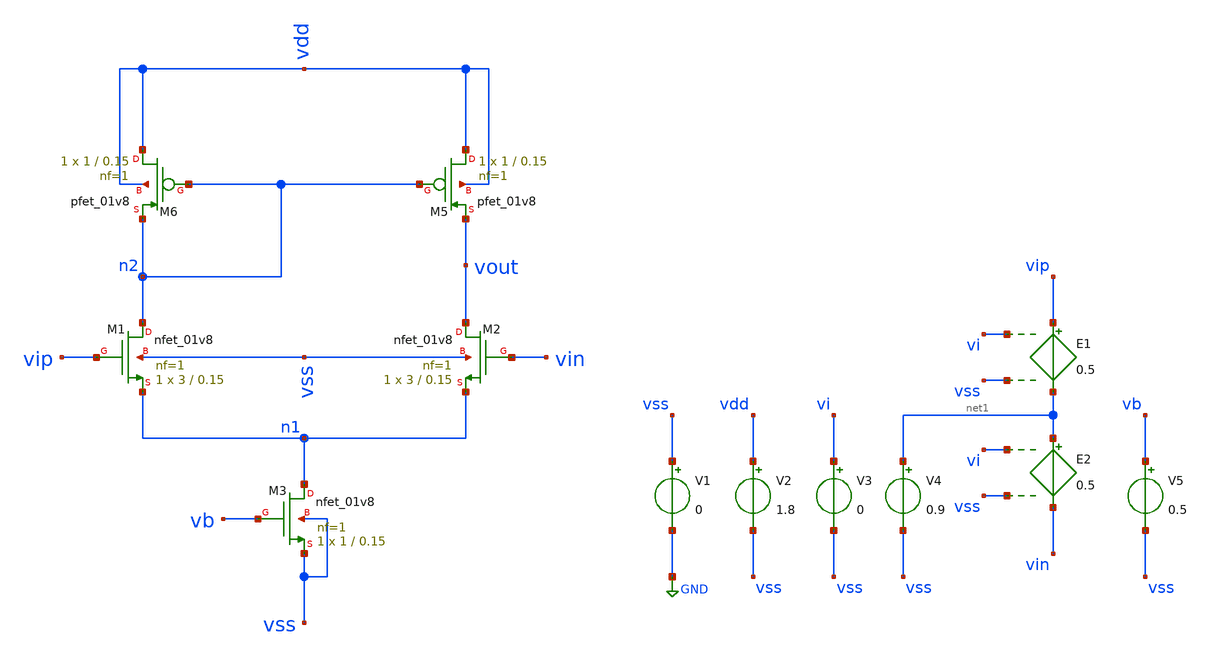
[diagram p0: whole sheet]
** sch_path: pre_layout_sim/ota_local_test.sch
**.subckt ota_local_test
XM1 n2 vip n1 vss sky130_fd_pr__nfet_01v8 L=0.15 W=3 nf=1 ad='int((1 + 1)/2) * 3 / 1 * 0.29' as='int((1 + 2)/2) * 3 / 1 * 0.29'
+ pd='2*int((1 + 1)/2) * (3 / 1 + 0.29)' ps='2*int((1 + 2)/2) * (3 / 1 + 0.29)' nrd='0.29 / 3 ' nrs='0.29 / 3 '
+ sa=0 sb=0 sd=0 mult=1 m=1
XM2 vout vin n1 vss sky130_fd_pr__nfet_01v8 L=0.15 W=3 nf=1 ad='int((1 + 1)/2) * 3 / 1 * 0.29' as='int((1 + 2)/2) * 3 / 1 * 0.29'
+ pd='2*int((1 + 1)/2) * (3 / 1 + 0.29)' ps='2*int((1 + 2)/2) * (3 / 1 + 0.29)' nrd='0.29 / 3 ' nrs='0.29 / 3 '
+ sa=0 sb=0 sd=0 mult=1 m=1
XM3 n1 vb vss vss sky130_fd_pr__nfet_01v8 L=0.15 W=1 nf=1 ad='int((1 + 1)/2) * 1 / 1 * 0.29' as='int((1 + 2)/2) * 1 / 1 * 0.29'
+ pd='2*int((1 + 1)/2) * (1 / 1 + 0.29)' ps='2*int((1 + 2)/2) * (1 / 1 + 0.29)' nrd='0.29 / 1 ' nrs='0.29 / 1 '
+ sa=0 sb=0 sd=0 mult=1 m=1
XM5 vdd n2 vout vdd sky130_fd_pr__pfet_01v8 L=0.15 W=1 nf=1 ad='int((1 + 1)/2) * 1 / 1 * 0.29' as='int((1 + 2)/2) * 1 / 1 * 0.29'
+ pd='2*int((1 + 1)/2) * (1 / 1 + 0.29)' ps='2*int((1 + 2)/2) * (1 / 1 + 0.29)' nrd='0.29 / 1 ' nrs='0.29 / 1 '
+ sa=0 sb=0 sd=0 mult=1 m=1
XM6 vdd n2 n2 vdd sky130_fd_pr__pfet_01v8 L=0.15 W=1 nf=1 ad='int((1 + 1)/2) * 1 / 1 * 0.29' as='int((1 + 2)/2) * 1 / 1 * 0.29'
+ pd='2*int((1 + 1)/2) * (1 / 1 + 0.29)' ps='2*int((1 + 2)/2) * (1 / 1 + 0.29)' nrd='0.29 / 1 ' nrs='0.29 / 1 '
+ sa=0 sb=0 sd=0 mult=1 m=1
V1 vss GND 0
V2 vdd vss 1.8
V3 vi vss 0
E1 vip net1 vi vss 0.5
V4 net1 vss 0.9
E2 net1 vin vi vss 0.5
V5 vb vss 0.5
**** begin user architecture code


.control
save all
save @m.xm1.msky130_fd_pr__nfet_01v8[id] @m.xm1.msky130_fd_pr__nfet_01v8[gm]
save @m.xm2.msky130_fd_pr__nfet_01v8[id] @m.xm2.msky130_fd_pr__nfet_01v8[gm]
save @m.xm3.msky130_fd_pr__nfet_01v8[id] @m.xm3.msky130_fd_pr__nfet_01v8[gm]
save @m.xm5.msky130_fd_pr__pfet_01v8[id] @m.xm5.msky130_fd_pr__pfet_01v8[gm]
save @m.xm6.msky130_fd_pr__pfet_01v8[id] @m.xm6.msky130_fd_pr__pfet_01v8[gm]
op
write ota_local_test.raw
.endc



** opencircuitdesign pdks install
.lib $::SKYWATER_MODELS/sky130.lib.spice tt

**** end user architecture code
**.ends
.GLOBAL GND
.end
